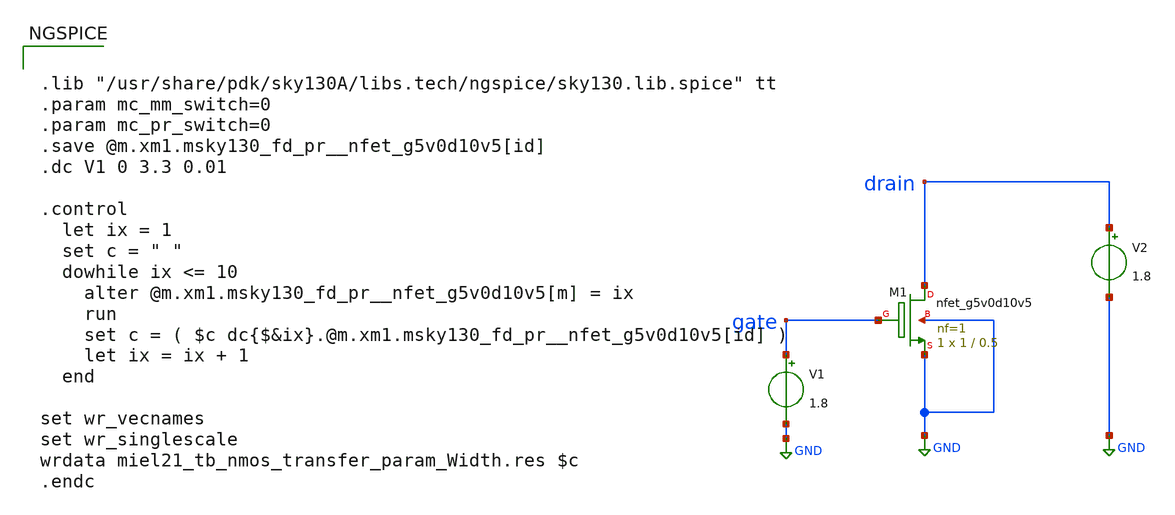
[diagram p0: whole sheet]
** sch_path: dev/opamp/miel21_tb_nmos_transfer_param_Width.sch
**.subckt miel21_tb_nmos_transfer_param_Width
V1 gate GND 1.8
V2 drain GND 1.8
XM1 drain gate GND GND sky130_fd_pr__nfet_g5v0d10v5 L=0.5 W=1 nf=1 ad='int((nf+1)/2) * W/nf * 0.29' as='int((nf+2)/2) * W/nf * 0.29'
+ pd='2*int((nf+1)/2) * (W/nf + 0.29)' ps='2*int((nf+2)/2) * (W/nf + 0.29)' nrd='0.29 / W' nrs='0.29 / W'
+ sa=0 sb=0 sd=0 mult=1 m=1
**** begin user architecture code


.lib "/usr/share/pdk/sky130A/libs.tech/ngspice/sky130.lib.spice" tt
.param mc_mm_switch=0
.param mc_pr_switch=0
.save @m.xm1.msky130_fd_pr__nfet_g5v0d10v5[id]
.dc V1 0 3.3 0.01

.control
  let ix = 1
  set c = " "
  dowhile ix <= 10
    alter @m.xm1.msky130_fd_pr__nfet_g5v0d10v5[m] = ix
    run
    set c = ( $c dc{$&ix}.@m.xm1.msky130_fd_pr__nfet_g5v0d10v5[id] )
    let ix = ix + 1
  end

set wr_vecnames
set wr_singlescale
wrdata miel21_tb_nmos_transfer_param_Width.res $c
.endc


**** end user architecture code
**.ends
.GLOBAL GND
.end
